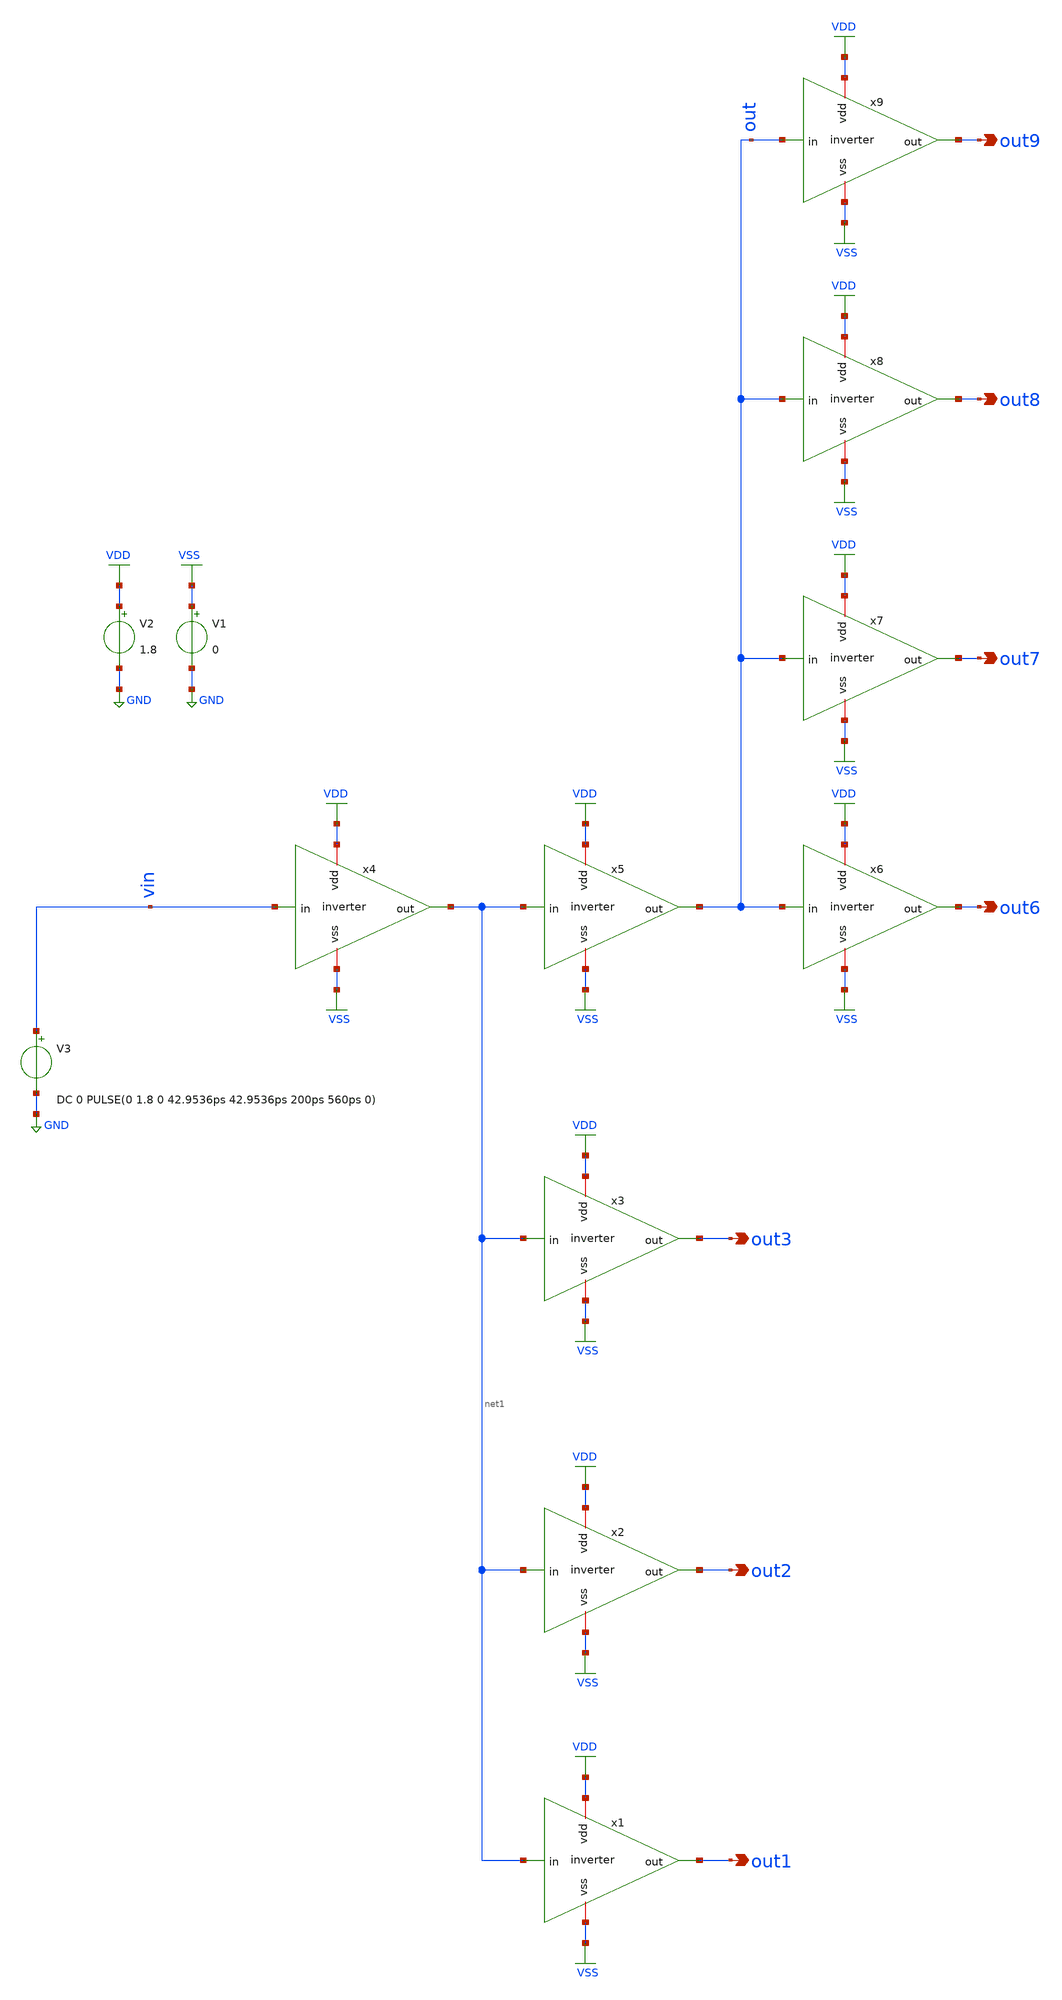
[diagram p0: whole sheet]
** sch_path: scripts/fo4/tb_fo4.sch
**.subckt tb_fo4 out7 out6 out8 out9 out3 out2 out1
*.opin out7
*.opin out6
*.opin out8
*.opin out9
*.opin out3
*.opin out2
*.opin out1
V1 VSS GND 0
V2 VDD GND 1.8
V3 vin GND

DC 0 PULSE(0 1.8 0 42.9536ps 42.9536ps 200ps 560ps 0)


x1 VDD out1 net1 VSS inverter
x2 VDD out2 net1 VSS inverter
x3 VDD out3 net1 VSS inverter
x4 VDD net1 vin VSS inverter
x5 VDD out net1 VSS inverter
x6 VDD out6 out VSS inverter
x7 VDD out7 out VSS inverter
x8 VDD out8 out VSS inverter
x9 VDD out9 out VSS inverter
**** begin user architecture code



.param pp = 1.85
.param pn = 0.41

********************************
* Control section
********************************
.control

* Voltage values to calculate rise and fall times
let v_steady = 1.8
let per10 = v_steady * 0.1
let per90 = v_steady * 0.9
let per50 = v_steady * 0.5

* These limits are based on the design of a standard cell of 12 tracks.
let wp_max = 1.85
let wn_min = 0.41
let wp_min = 0.42
let wn_max = 1.84

* Initialization of variables and size of iteration.
let delta_w = 0.01
let wp = wp_max
let wn = wn_min
let loop = 0

* These vector will be used to save the data of each iteration.
let loops = (wp_max-wp_min)/0.01
let wpv = unitvec($&loops)
let wnv = unitvec($&loops)
let trv = unitvec($&loops)
let tfv = unitvec($&loops)

* Start loop
while wp ge wp_min

* Modify widths
  echo
  echo ********************************** Cycle $&loop **********************************
  echo
  alterparam pp = $&wp
  reset
  alterparam pn = $&wn
  reset

* Run transient analysis
  TRAN 1p 1.68n $ 3 periods

* Find rise and fall times
  echo
  meas  TRAN  t_rise  TRIG  v(out) VAL=per10 RISE=2  TARG v(out)  VAL=per90 RISE=2
  meas  TRAN  t_fall  TRIG  v(out) VAL=per90 FALL=2  TARG v(out)  VAL=per10 FALL=2
  echo Wn: $&wn
  echo Wp: $&wp
  echo

* Save widths, t_rise, t_fall in vectors
  let wnv[loop] = wn
  let wpv[loop] = wp
  let trv[loop] = t_rise
  let tfv[loop] = t_fall

* Modify widths
  let wn = wn + delta_w
  let wp = wp - delta_w

* Counter increment
  let loop = loop + 1

end

echo
echo ********************************** End of Simulation **********************************
echo

* Export vector data into raw file
write data_VACIO.raw wnv wpv trv tfv

* Plot both rise and fall times vs. NMOS widths
* plot trv vs wnv, tfv vs wnv
.endc






.lib $::SKYWATER_MODELS/sky130.lib.spice VACIO

.param mc_mm_switch=0
.param mc_pr_switch=1


**** end user architecture code
**.ends

* expanding   symbol:  inverter.sym # of pins=4
** sym_path: scripts/fo4/inverter.sym
** sch_path: scripts/fo4/inverter.sch
.subckt inverter vdd out in vss
*.opin out
*.ipin in
*.iopin vdd
*.iopin vss
XM1 out in vdd vdd sky130_fd_pr__pfet_01v8 L=0.15 W=pp nf=1 ad='int((nf+1)/2) * W/nf * 0.29' as='int((nf+2)/2) * W/nf * 0.29'
+ pd='2*int((nf+1)/2) * (W/nf + 0.29)' ps='2*int((nf+2)/2) * (W/nf + 0.29)' nrd='0.29 / W' nrs='0.29 / W'
+ sa=0 sb=0 sd=0 mult=1 m=1
XM2 out in vss vss sky130_fd_pr__nfet_01v8 L=0.15 W=pn nf=1 ad='int((nf+1)/2) * W/nf * 0.29' as='int((nf+2)/2) * W/nf * 0.29'
+ pd='2*int((nf+1)/2) * (W/nf + 0.29)' ps='2*int((nf+2)/2) * (W/nf + 0.29)' nrd='0.29 / W' nrs='0.29 / W'
+ sa=0 sb=0 sd=0 mult=1 m=1
.ends

.GLOBAL VSS
.GLOBAL VDD
.GLOBAL GND
.end
